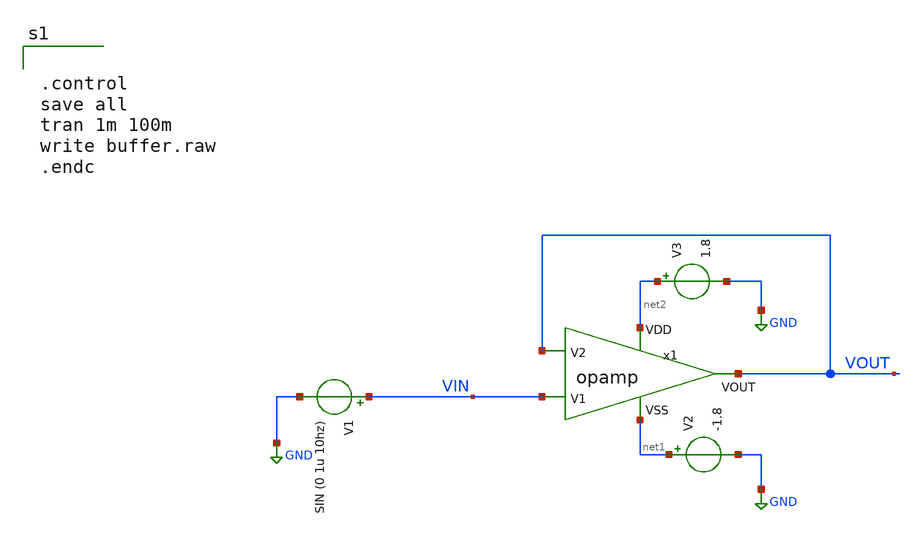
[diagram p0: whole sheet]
** sch_path: buffer.sch
**.subckt buffer
V3 net2 GND 1.8
V2 net1 GND -1.8
x1 net2 net1 VIN VOUT VOUT opamp
V1 VIN GND SIN (0 1u 10hz)
**** begin user architecture code

** opencircuitdesign pdks install
.lib $::SKYWATER_MODELS/sky130.lib.spice tt




.control
save all
tran 1m 100m
write buffer.raw
.endc


**** end user architecture code
**.ends

* expanding   symbol:  /foss/designs/sky130_hcmus_ip__instramp/xschem/opamp.sym # of pins=5
** sym_path: /foss/designs/sky130_hcmus_ip__instramp/xschem/opamp.sym
** sch_path: /foss/designs/sky130_hcmus_ip__instramp/xschem/opamp.sch
.subckt opamp VDD VSS V1 V2 VOUT
*.ipin VSS
*.ipin VDD
*.ipin V2
*.ipin V1
*.opin VOUT
XM3 net4 V2 net1 VSS sky130_fd_pr__nfet_g5v0d10v5 L=1 W=17.45 nf=1 ad='int((nf+1)/2) * W/nf * 0.29' as='int((nf+2)/2) * W/nf * 0.29'
+ pd='2*int((nf+1)/2) * (W/nf + 0.29)' ps='2*int((nf+2)/2) * (W/nf + 0.29)' nrd='0.29 / W' nrs='0.29 / W'
+ sa=0 sb=0 sd=0 mult=1 m=1
XM1 net5 net4 VDD VDD sky130_fd_pr__pfet_g5v0d10v5 L=1 W=30 nf=1 ad='int((nf+1)/2) * W/nf * 0.29' as='int((nf+2)/2) * W/nf * 0.29'
+ pd='2*int((nf+1)/2) * (W/nf + 0.29)' ps='2*int((nf+2)/2) * (W/nf + 0.29)' nrd='0.29 / W' nrs='0.29 / W'
+ sa=0 sb=0 sd=0 mult=1 m=1
XM4 net5 V1 net1 VSS sky130_fd_pr__nfet_g5v0d10v5 L=1 W=17.45 nf=1 ad='int((nf+1)/2) * W/nf * 0.29' as='int((nf+2)/2) * W/nf * 0.29'
+ pd='2*int((nf+1)/2) * (W/nf + 0.29)' ps='2*int((nf+2)/2) * (W/nf + 0.29)' nrd='0.29 / W' nrs='0.29 / W'
+ sa=0 sb=0 sd=0 mult=1 m=1
XM6 net1 net6 VSS VSS sky130_fd_pr__nfet_g5v0d10v5 L=1 W=15.17 nf=1 ad='int((nf+1)/2) * W/nf * 0.29'
+ as='int((nf+2)/2) * W/nf * 0.29' pd='2*int((nf+1)/2) * (W/nf + 0.29)' ps='2*int((nf+2)/2) * (W/nf + 0.29)'
+ nrd='0.29 / W' nrs='0.29 / W' sa=0 sb=0 sd=0 mult=1 m=1
XM7 VOUT net6 VSS VSS sky130_fd_pr__nfet_g5v0d10v5 L=1 W=19 nf=1 ad='int((nf+1)/2) * W/nf * 0.29' as='int((nf+2)/2) * W/nf * 0.29'
+ pd='2*int((nf+1)/2) * (W/nf + 0.29)' ps='2*int((nf+2)/2) * (W/nf + 0.29)' nrd='0.29 / W' nrs='0.29 / W'
+ sa=0 sb=0 sd=0 mult=1 m=1
XM5 net6 net6 VSS VSS sky130_fd_pr__nfet_g5v0d10v5 L=1 W=15.17 nf=1 ad='int((nf+1)/2) * W/nf * 0.29'
+ as='int((nf+2)/2) * W/nf * 0.29' pd='2*int((nf+1)/2) * (W/nf + 0.29)' ps='2*int((nf+2)/2) * (W/nf + 0.29)'
+ nrd='0.29 / W' nrs='0.29 / W' sa=0 sb=0 sd=0 mult=1 m=1
XM2 net4 net4 VDD VDD sky130_fd_pr__pfet_g5v0d10v5 L=1 W=30 nf=1 ad='int((nf+1)/2) * W/nf * 0.29' as='int((nf+2)/2) * W/nf * 0.29'
+ pd='2*int((nf+1)/2) * (W/nf + 0.29)' ps='2*int((nf+2)/2) * (W/nf + 0.29)' nrd='0.29 / W' nrs='0.29 / W'
+ sa=0 sb=0 sd=0 mult=1 m=1
XM8 VOUT net5 VDD VDD sky130_fd_pr__pfet_g5v0d10v5 L=1 W=38 nf=1 ad='int((nf+1)/2) * W/nf * 0.29' as='int((nf+2)/2) * W/nf * 0.29'
+ pd='2*int((nf+1)/2) * (W/nf + 0.29)' ps='2*int((nf+2)/2) * (W/nf + 0.29)' nrd='0.29 / W' nrs='0.29 / W'
+ sa=0 sb=0 sd=0 mult=2 m=2
V_ibias net7 net6 0
.save i(v_ibias)
XR1 net2 VDD VSS sky130_fd_pr__res_high_po W=1 L=41.1 mult=1 m=1
XR2 net3 net2 VSS sky130_fd_pr__res_high_po W=1 L=41.1 mult=1 m=1
XR3 net7 net3 VSS sky130_fd_pr__res_high_po W=1 L=41.1 mult=1 m=1
XR4 net8 VOUT VSS sky130_fd_pr__res_high_po W=1 L=5 mult=1 m=1
XC1 net8 net5 sky130_fd_pr__cap_mim_m3_1 W=9 L=9 MF=2 m=2
.ends

.GLOBAL GND
.end
